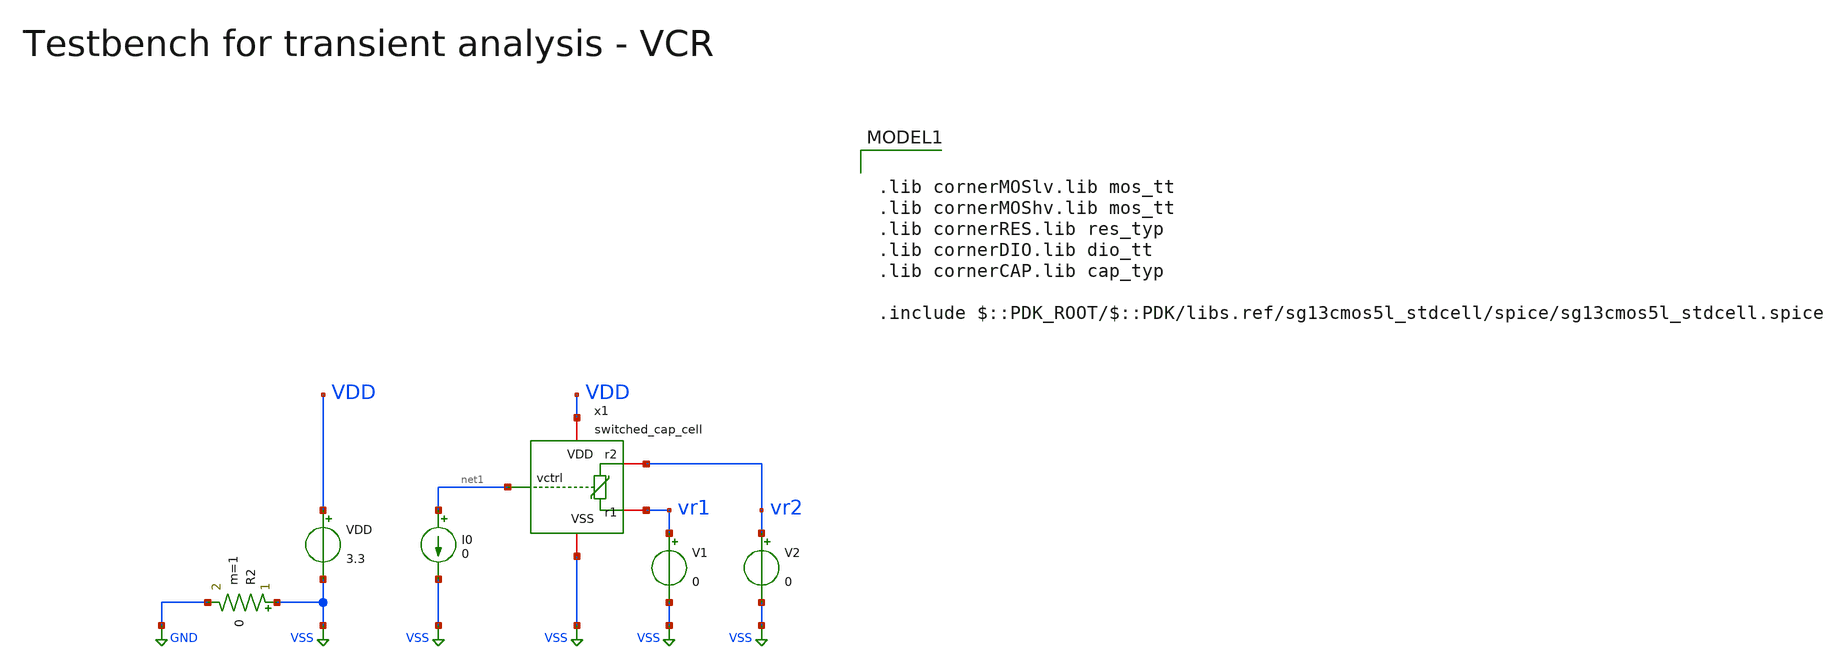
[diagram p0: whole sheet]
** sch_path: macros/heichips26_vcr/macros/switched_capacitor/testbenches/xschem/tb_switched_cap_tran_sweep.sch
**.subckt tb_switched_cap_tran_sweep
VDD VDD VSS 3.3
R2 VSS GND 0 m=1
I0 net1 VSS 0
x1 net1 VDD VSS vr2 vr1 switched_cap_cell
V1 vr1 VSS 0
V2 vr2 VSS 0
**** begin user architecture code

.lib cornerMOSlv.lib mos_tt
.lib cornerMOShv.lib mos_tt
.lib cornerRES.lib res_typ
.lib cornerDIO.lib dio_tt
.lib cornerCAP.lib cap_typ

.include $::PDK_ROOT/$::PDK/libs.ref/sg13cmos5l_stdcell/spice/sg13cmos5l_stdcell.spice



.param temp=27

* Derived timing parameters

.options savecurrents klu method=gear reltol=1e-3 abstol=1e-12 gmin=1e-15
.probe alli
.control

echo
echo # ------------------------------------------------------------------------------
echo # VCM sweep:
echo # ------------------------------------------------------------------------------
echo

unset appendwrite
set wr_vecnames
set wr_singlescale

let vdd_var = 3.3
let record_periods = 5
let i_to_f = 3.3e-12
let ictrl = 1u

set currents = ( 3.3u 33u 330u )
foreach ictrl $currents
break
	let f = $ictrl/i_to_f
	let period = 1/f
	let tstop = record_periods*period
	let tstep = period/100
	echo ictrl=$ictrl, f=$&f, period=$&period, tstop=$&tstop, tstep=$&tstep
	alter i0 = $ictrl

	let vdm = 0.5
	let vcm = 0.3
	while vcm <= 3
		let v1 = $&vcm - $&vdm/2
		let v2 = $&vcm + $&vdm/2
		echo vcm=$&vcm, vdm=$&vdm, v1=$&v1, v2=$&v2
		alter v1 = $&v1
		alter v2 = $&v2
		tran $&tstep $&tstop
		wrdata ../plot_simulations/data/@schname\_vcm.txt i(i0) i(v1) vr1 vr2
		set appendwrite
		unset wr_vecnames
		let vcm = $&vcm + 0.1
	end
end

echo
echo # ------------------------------------------------------------------------------
echo # VDM sweep:
echo # ------------------------------------------------------------------------------
echo

unset appendwrite
set wr_vecnames

set currents = ( 3.3u 33u 330u )
foreach ictrl $currents
break
	let f = $ictrl/i_to_f
	let period = 1/f
	let tstop = record_periods*period
	let tstep = period/100
	echo ictrl=$ictrl, f=$&f, period=$&period, tstop=$&tstop, tstep=$&tstep
	alter i0 = $ictrl

	let vdm = 0.1
	let vcm = $&vdd_var/2
	while vdm < $&vdd_var
		let v1 = $&vcm - $&vdm/2
		let v2 = $&vcm + $&vdm/2
		echo ictrl=$ictrl, vcm=$&vcm, vdm=$&vdm, v1=$&v1, v2=$&v2
		alter v1 = $&v1
		alter v2 = $&v2
		tran $&tstep $&tstop
		wrdata ../plot_simulations/data/@schname\_vdm.txt i(i0) i(v1) vr1 vr2
		set appendwrite
		unset wr_vecnames
		let vdm = vdm + 0.1
	end
end

echo
echo # ------------------------------------------------------------------------------
echo # Ictrl sweep:
echo # ------------------------------------------------------------------------------
echo

unset appendwrite
set wr_vecnames

let vdm = $&vdd_var/2
let vcm = $&vdd_var/2
let v1 = $&vcm - $&vdm/2
let v2 = $&vcm + $&vdm/2
echo v1=$&v1, v2=$&v2
alter v1 $&v1
alter v2 $&v2

while $&ictrl < 400u
	let f = $&ictrl/i_to_f
	let period = 1/f
	let tstop = record_periods*period
	let tstep = period/100
	echo ictrl=$&ictrl, f=$&f, period=$&period, tstop=$&tstop, tstep=$&tstep

	alter i0 = $&ictrl
	tran $&tstep $&tstop
	wrdata ../plot_simulations/data/@schname\_ictrl.txt i(i0) i(v1) vr1 vr2
	set appendwrite
	unset wr_vecnames
	let ictrl = ictrl * 1.1
end

*quit
.endc


**** end user architecture code
**.ends
.GLOBAL VSS
.GLOBAL GND
.end
